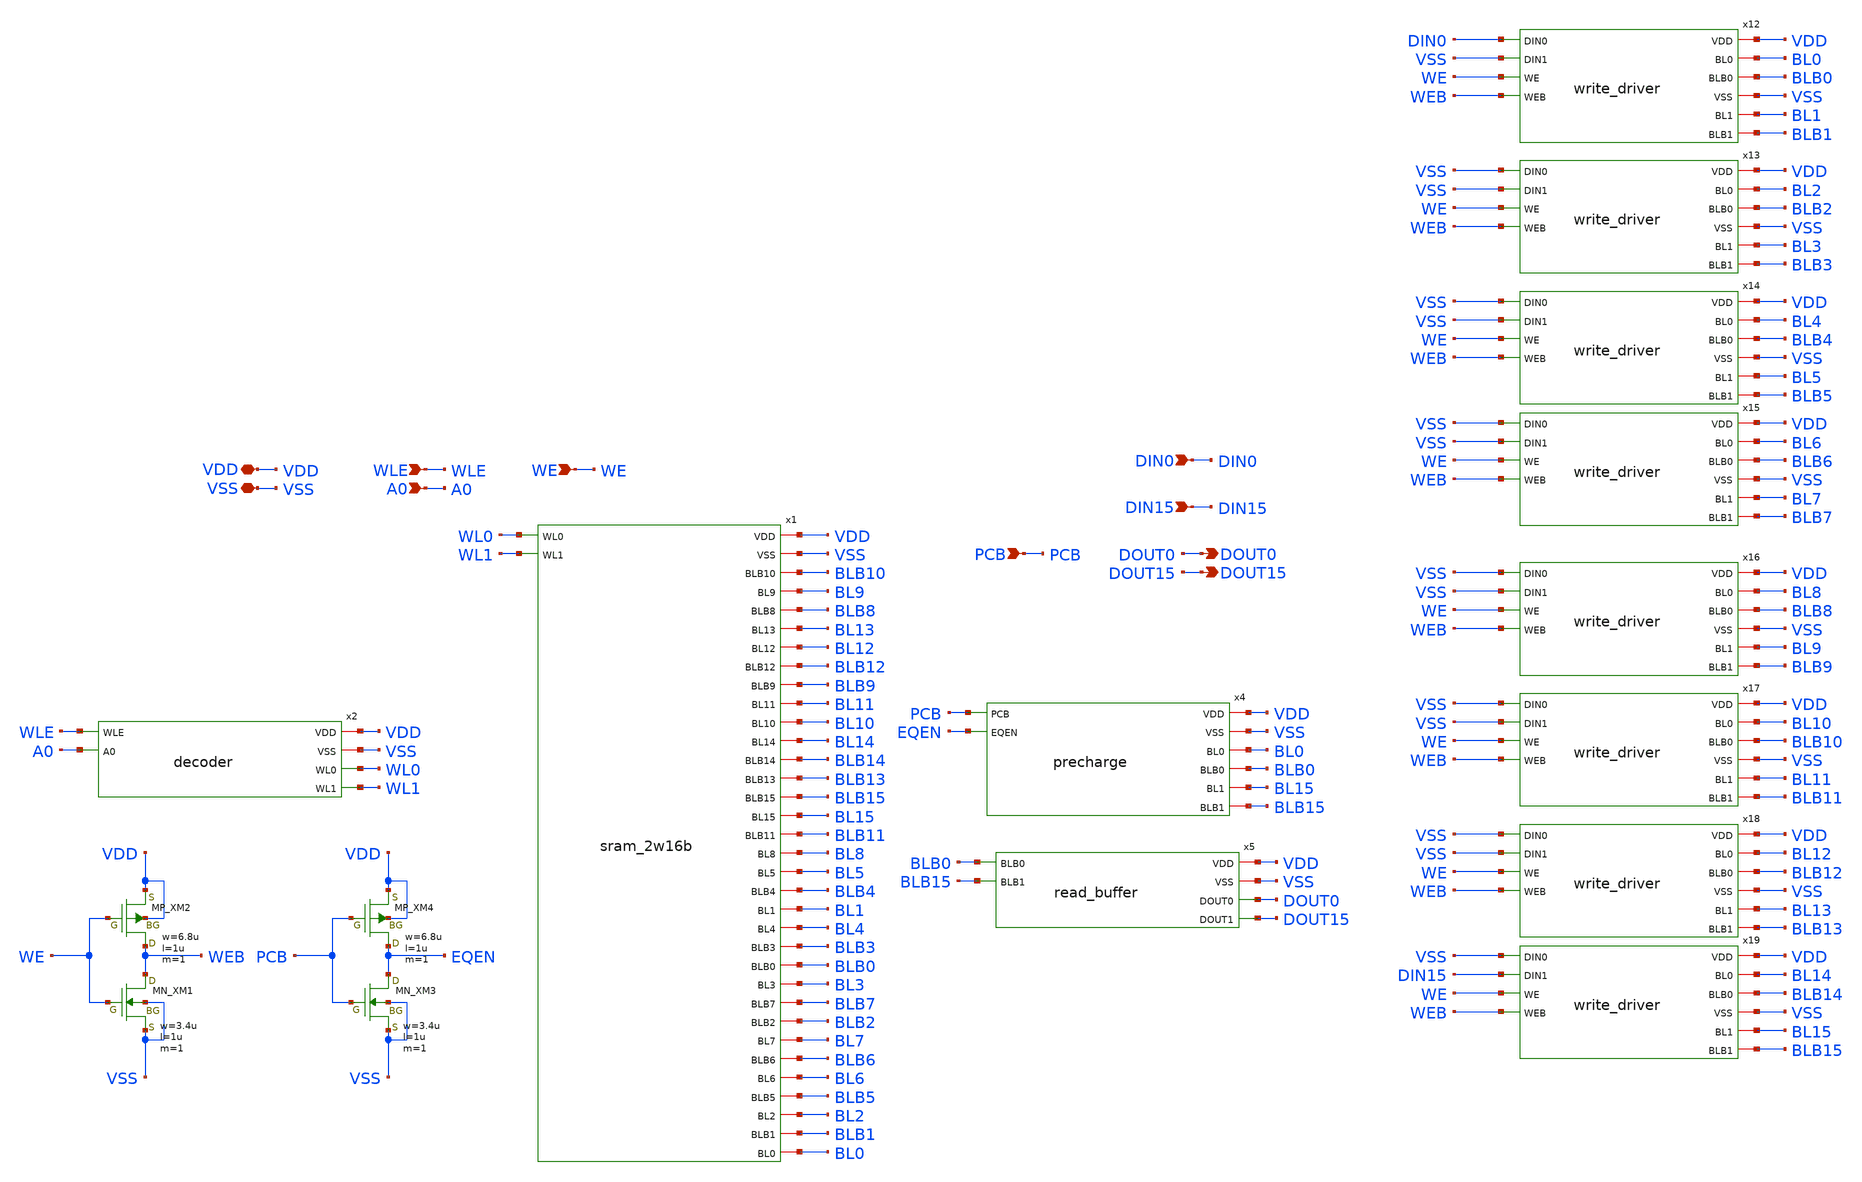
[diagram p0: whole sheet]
** sch_path: sram/sram_2w16b_top.sch
**.subckt sram_2w16b_top VDD WLE DOUT0 VSS A0 WE DIN0 PCB DOUT15 DIN15
*.iopin VDD
*.ipin WLE
*.opin DOUT0
*.iopin VSS
*.ipin A0
*.ipin WE
*.ipin DIN0
*.ipin PCB
*.opin DOUT15
*.ipin DIN15
x2 VDD VSS WL0 WLE A0 WL1 decoder
x4 VDD VSS PCB EQEN BL0 BLB0 BL15 BLB15 precharge
x5 VDD VSS BLB0 BLB15 DOUT0 DOUT15 read_buffer
XXM1 WEB WE VSS VSS NMOS w=3.4u l=1u nrd=0 nrs=0 m=1
XXM2 WEB WE VDD VDD PMOS w=6.8u l=1u nrd=0 nrs=0 m=1
XXM3 EQEN PCB VSS VSS NMOS w=3.4u l=1u nrd=0 nrs=0 m=1
XXM4 EQEN PCB VDD VDD PMOS w=6.8u l=1u nrd=0 nrs=0 m=1
x1 WL0 VDD VSS WL1 BLB10 BL9 BLB8 BL13 BL12 BLB12 BLB9 BL11 BL10 BL14 BLB14 BLB13 BLB15 BL15 BLB11
+ BL8 BL5 BLB4 BL1 BL4 BLB3 BLB0 BL3 BLB7 BLB2 BL7 BLB6 BL6 BLB5 BL2 BLB1 BL0 sram_2w16b
x12 DIN0 VDD BL0 BLB0 VSS VSS BL1 WE BLB1 WEB write_driver
x13 VSS VDD BL2 BLB2 VSS VSS BL3 WE BLB3 WEB write_driver
x14 VSS VDD BL4 BLB4 VSS VSS BL5 WE BLB5 WEB write_driver
x15 VSS VDD BL6 BLB6 VSS VSS BL7 WE BLB7 WEB write_driver
x16 VSS VDD BL8 BLB8 VSS VSS BL9 WE BLB9 WEB write_driver
x17 VSS VDD BL10 BLB10 VSS VSS BL11 WE BLB11 WEB write_driver
x18 VSS VDD BL12 BLB12 VSS VSS BL13 WE BLB13 WEB write_driver
x19 VSS VDD BL14 BLB14 VSS DIN15 BL15 WE BLB15 WEB write_driver
**.ends
.end
